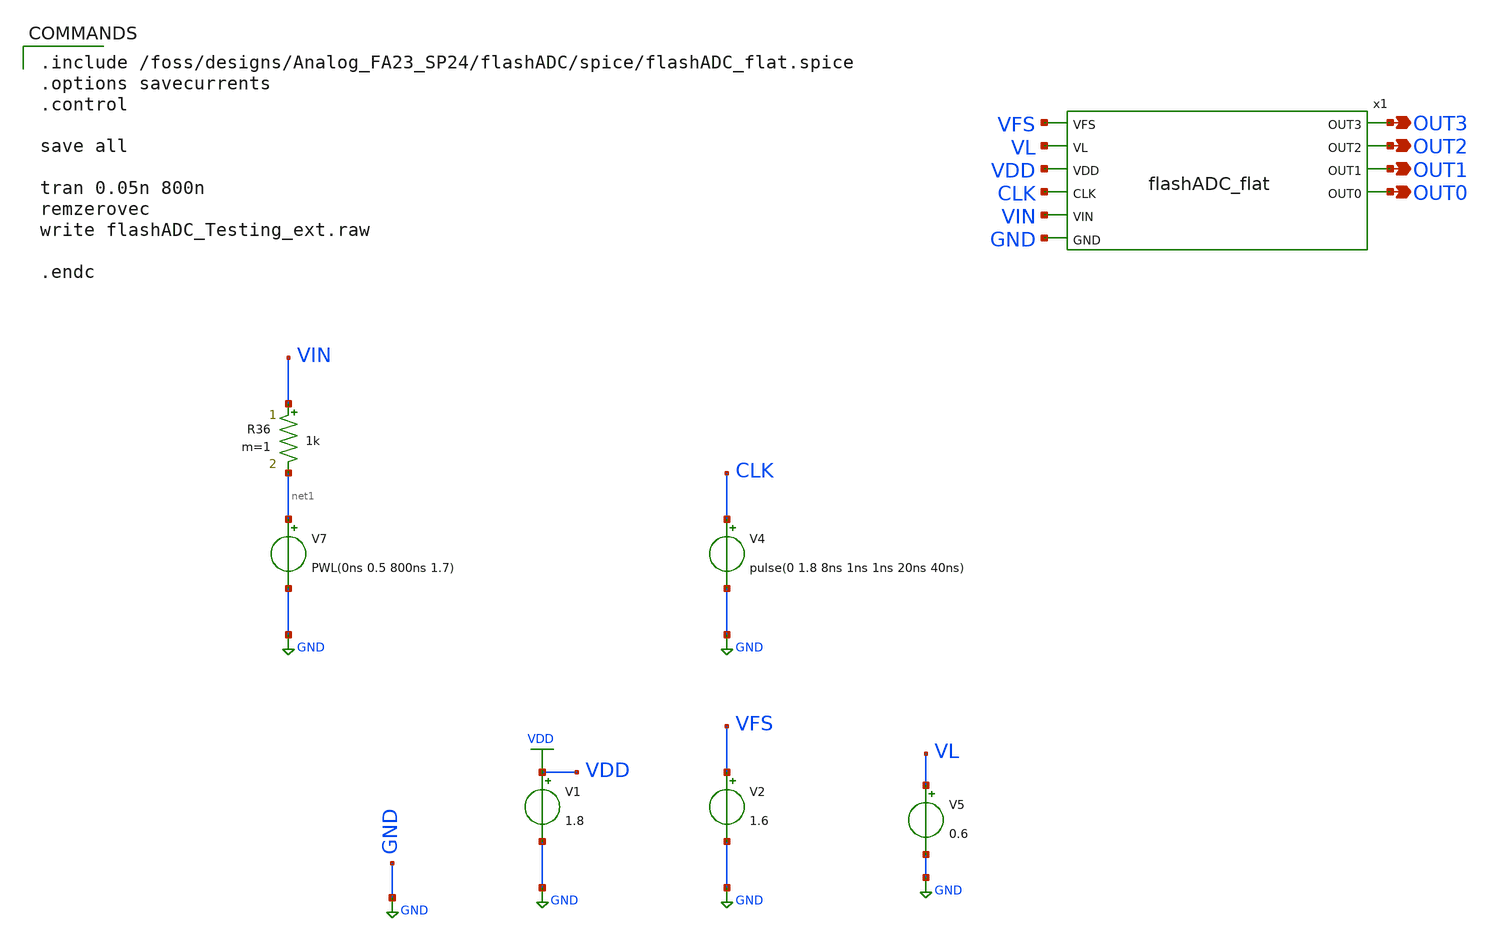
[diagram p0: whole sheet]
** sch_path: flashADC/xschem/flashADC_Testing_ext.sch
.lib $::SKYWATER_MODELS/sky130.lib.spice tt
.include $::SKYWATER_STDCELLS/sky130_fd_sc_hd.spice

**.subckt flashADC_Testing_ext OUT3 OUT2 OUT1 OUT0
*.opin OUT3
*.opin OUT2
*.opin OUT1
*.opin OUT0
V4 CLK GND pulse(0 1.8 8ns 1ns 1ns 20ns 40ns)
V1 VDD GND 1.8
V2 VFS GND 1.6
V5 VL GND 0.6
V7 net1 GND PWL(0ns 0.5 800ns 1.7)
R36 VIN net1 1k m=1
x1 VFS OUT3 OUT2 OUT1 OUT0 VL VDD CLK VIN GND flashADC_flat
**** begin user architecture code

.include /foss/designs/Analog_FA23_SP24/flashADC/spice/flashADC_flat.spice
.options savecurrents
.control

save all

tran 0.05n 800n
remzerovec
write flashADC_Testing_ext.raw

.endc


**** end user architecture code
**.ends
.GLOBAL GND
.GLOBAL VDD
.end
